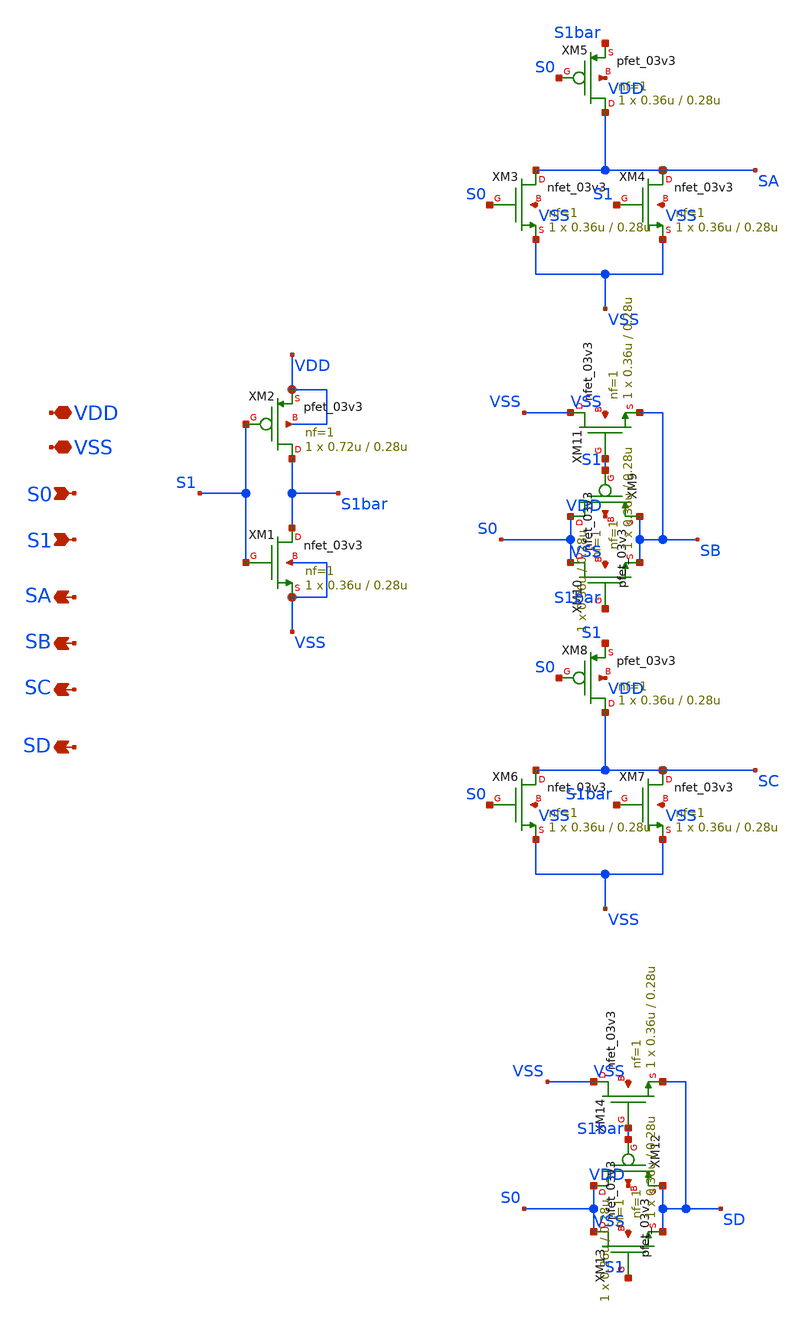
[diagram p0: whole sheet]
** sch_path: CAD4/2x4_decoder.sch
**.subckt 2x4_decoder S0 S1 SA SB SC SD VSS VDD
*.ipin S0
*.ipin S1
*.opin SA
*.opin SB
*.opin SC
*.opin SD
*.iopin VSS
*.iopin VDD
XM1 S1bar S1 VSS VSS nfet_03v3 L=0.28u W=0.36u nf=1 ad='int((nf+1)/2) * W/nf * 0.18u' as='int((nf+2)/2) * W/nf * 0.18u'
+ pd='2*int((nf+1)/2) * (W/nf + 0.18u)' ps='2*int((nf+2)/2) * (W/nf + 0.18u)' nrd='0.18u / W' nrs='0.18u / W'
+ sa=0 sb=0 sd=0 m=1
XM2 S1bar S1 VDD VDD pfet_03v3 L=0.28u W=0.72u nf=1 ad='int((nf+1)/2) * W/nf * 0.18u' as='int((nf+2)/2) * W/nf * 0.18u'
+ pd='2*int((nf+1)/2) * (W/nf + 0.18u)' ps='2*int((nf+2)/2) * (W/nf + 0.18u)' nrd='0.18u / W' nrs='0.18u / W'
+ sa=0 sb=0 sd=0 m=1
XM3 SA S0 VSS VSS nfet_03v3 L=0.28u W=0.36u nf=1 ad='int((nf+1)/2) * W/nf * 0.18u' as='int((nf+2)/2) * W/nf * 0.18u'
+ pd='2*int((nf+1)/2) * (W/nf + 0.18u)' ps='2*int((nf+2)/2) * (W/nf + 0.18u)' nrd='0.18u / W' nrs='0.18u / W'
+ sa=0 sb=0 sd=0 m=1
XM4 SA S1 VSS VSS nfet_03v3 L=0.28u W=0.36u nf=1 ad='int((nf+1)/2) * W/nf * 0.18u' as='int((nf+2)/2) * W/nf * 0.18u'
+ pd='2*int((nf+1)/2) * (W/nf + 0.18u)' ps='2*int((nf+2)/2) * (W/nf + 0.18u)' nrd='0.18u / W' nrs='0.18u / W'
+ sa=0 sb=0 sd=0 m=1
XM5 SA S0 S1bar VDD pfet_03v3 L=0.28u W=0.36u nf=1 ad='int((nf+1)/2) * W/nf * 0.18u' as='int((nf+2)/2) * W/nf * 0.18u'
+ pd='2*int((nf+1)/2) * (W/nf + 0.18u)' ps='2*int((nf+2)/2) * (W/nf + 0.18u)' nrd='0.18u / W' nrs='0.18u / W'
+ sa=0 sb=0 sd=0 m=1
XM9 S0 S1 SB VDD pfet_03v3 L=0.28u W=0.36u nf=1 ad='int((nf+1)/2) * W/nf * 0.18u' as='int((nf+2)/2) * W/nf * 0.18u'
+ pd='2*int((nf+1)/2) * (W/nf + 0.18u)' ps='2*int((nf+2)/2) * (W/nf + 0.18u)' nrd='0.18u / W' nrs='0.18u / W'
+ sa=0 sb=0 sd=0 m=1
XM10 S0 S1bar SB VSS nfet_03v3 L=0.28u W=0.36u nf=1 ad='int((nf+1)/2) * W/nf * 0.18u' as='int((nf+2)/2) * W/nf * 0.18u'
+ pd='2*int((nf+1)/2) * (W/nf + 0.18u)' ps='2*int((nf+2)/2) * (W/nf + 0.18u)' nrd='0.18u / W' nrs='0.18u / W'
+ sa=0 sb=0 sd=0 m=1
XM11 VSS S1 SB VSS nfet_03v3 L=0.28u W=0.36u nf=1 ad='int((nf+1)/2) * W/nf * 0.18u' as='int((nf+2)/2) * W/nf * 0.18u'
+ pd='2*int((nf+1)/2) * (W/nf + 0.18u)' ps='2*int((nf+2)/2) * (W/nf + 0.18u)' nrd='0.18u / W' nrs='0.18u / W'
+ sa=0 sb=0 sd=0 m=1
XM12 S0 S1bar SD VDD pfet_03v3 L=0.28u W=0.36u nf=1 ad='int((nf+1)/2) * W/nf * 0.18u' as='int((nf+2)/2) * W/nf * 0.18u'
+ pd='2*int((nf+1)/2) * (W/nf + 0.18u)' ps='2*int((nf+2)/2) * (W/nf + 0.18u)' nrd='0.18u / W' nrs='0.18u / W'
+ sa=0 sb=0 sd=0 m=1
XM13 S0 S1 SD VSS nfet_03v3 L=0.28u W=0.36u nf=1 ad='int((nf+1)/2) * W/nf * 0.18u' as='int((nf+2)/2) * W/nf * 0.18u'
+ pd='2*int((nf+1)/2) * (W/nf + 0.18u)' ps='2*int((nf+2)/2) * (W/nf + 0.18u)' nrd='0.18u / W' nrs='0.18u / W'
+ sa=0 sb=0 sd=0 m=1
XM14 VSS S1bar SD VSS nfet_03v3 L=0.28u W=0.36u nf=1 ad='int((nf+1)/2) * W/nf * 0.18u' as='int((nf+2)/2) * W/nf * 0.18u'
+ pd='2*int((nf+1)/2) * (W/nf + 0.18u)' ps='2*int((nf+2)/2) * (W/nf + 0.18u)' nrd='0.18u / W' nrs='0.18u / W'
+ sa=0 sb=0 sd=0 m=1
XM6 SC S0 VSS VSS nfet_03v3 L=0.28u W=0.36u nf=1 ad='int((nf+1)/2) * W/nf * 0.18u' as='int((nf+2)/2) * W/nf * 0.18u'
+ pd='2*int((nf+1)/2) * (W/nf + 0.18u)' ps='2*int((nf+2)/2) * (W/nf + 0.18u)' nrd='0.18u / W' nrs='0.18u / W'
+ sa=0 sb=0 sd=0 m=1
XM7 SC S1bar VSS VSS nfet_03v3 L=0.28u W=0.36u nf=1 ad='int((nf+1)/2) * W/nf * 0.18u' as='int((nf+2)/2) * W/nf * 0.18u'
+ pd='2*int((nf+1)/2) * (W/nf + 0.18u)' ps='2*int((nf+2)/2) * (W/nf + 0.18u)' nrd='0.18u / W' nrs='0.18u / W'
+ sa=0 sb=0 sd=0 m=1
XM8 SC S0 S1 VDD pfet_03v3 L=0.28u W=0.36u nf=1 ad='int((nf+1)/2) * W/nf * 0.18u' as='int((nf+2)/2) * W/nf * 0.18u'
+ pd='2*int((nf+1)/2) * (W/nf + 0.18u)' ps='2*int((nf+2)/2) * (W/nf + 0.18u)' nrd='0.18u / W' nrs='0.18u / W'
+ sa=0 sb=0 sd=0 m=1
**.ends
.end
